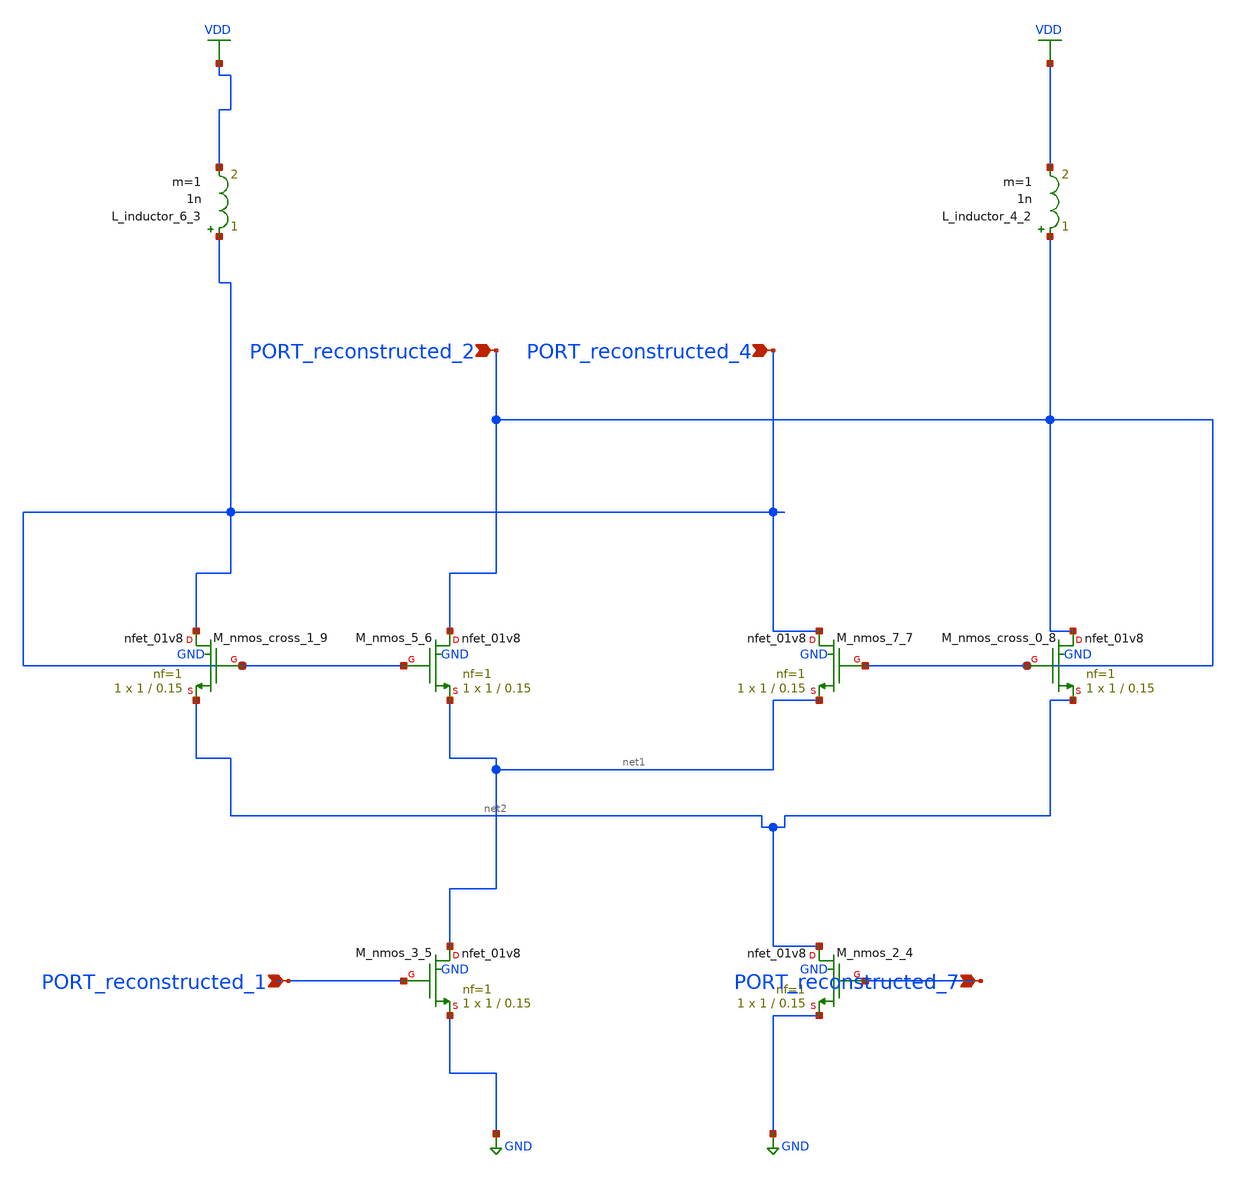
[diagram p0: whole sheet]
** sch_path: schematics/10_1007_s10470-024-02258-z_02_001.sch
**.subckt 10_1007_s10470-024-02258-z_02_001 PORT_reconstructed_2 PORT_reconstructed_1
*+ PORT_reconstructed_4 PORT_reconstructed_7
*.ipin PORT_reconstructed_2
*.ipin PORT_reconstructed_1
*.ipin PORT_reconstructed_4
*.ipin PORT_reconstructed_7
L_inductor_4_2 PORT_reconstructed_2 VDD 1n m=1
L_inductor_6_3 PORT_reconstructed_4 VDD 1n m=1
XM_nmos_2_4 net2 PORT_reconstructed_7 GND GND sky130_fd_pr__nfet_01v8 L=0.15 W=1 nf=1 ad='int((1 + 1)/2) * 1 / 1 * 0.29'
+ as='int((1 + 2)/2) * 1 / 1 * 0.29' pd='2*int((1 + 1)/2) * (1 / 1 + 0.29)' ps='2*int((1 + 2)/2) * (1 / 1 + 0.29)'
+ nrd='0.29 / 1 ' nrs='0.29 / 1 ' sa=0 sb=0 sd=0 mult=1 m=1
XM_nmos_3_5 net1 PORT_reconstructed_1 GND GND sky130_fd_pr__nfet_01v8 L=0.15 W=1 nf=1 ad='int((1 + 1)/2) * 1 / 1 * 0.29'
+ as='int((1 + 2)/2) * 1 / 1 * 0.29' pd='2*int((1 + 1)/2) * (1 / 1 + 0.29)' ps='2*int((1 + 2)/2) * (1 / 1 + 0.29)'
+ nrd='0.29 / 1 ' nrs='0.29 / 1 ' sa=0 sb=0 sd=0 mult=1 m=1
XM_nmos_5_6 PORT_reconstructed_2 PORT_reconstructed_4 net1 GND sky130_fd_pr__nfet_01v8 L=0.15 W=1 nf=1
+ ad='int((1 + 1)/2) * 1 / 1 * 0.29' as='int((1 + 2)/2) * 1 / 1 * 0.29' pd='2*int((1 + 1)/2) * (1 / 1 + 0.29)'
+ ps='2*int((1 + 2)/2) * (1 / 1 + 0.29)' nrd='0.29 / 1 ' nrs='0.29 / 1 ' sa=0 sb=0 sd=0 mult=1 m=1
XM_nmos_7_7 PORT_reconstructed_4 PORT_reconstructed_2 net1 GND sky130_fd_pr__nfet_01v8 L=0.15 W=1 nf=1
+ ad='int((1 + 1)/2) * 1 / 1 * 0.29' as='int((1 + 2)/2) * 1 / 1 * 0.29' pd='2*int((1 + 1)/2) * (1 / 1 + 0.29)'
+ ps='2*int((1 + 2)/2) * (1 / 1 + 0.29)' nrd='0.29 / 1 ' nrs='0.29 / 1 ' sa=0 sb=0 sd=0 mult=1 m=1
XM_nmos_cross_0_8 PORT_reconstructed_2 PORT_reconstructed_2 net2 GND sky130_fd_pr__nfet_01v8 L=0.15 W=1
+ nf=1 ad='int((1 + 1)/2) * 1 / 1 * 0.29' as='int((1 + 2)/2) * 1 / 1 * 0.29' pd='2*int((1 + 1)/2) * (1 / 1 + 0.29)'
+ ps='2*int((1 + 2)/2) * (1 / 1 + 0.29)' nrd='0.29 / 1 ' nrs='0.29 / 1 ' sa=0 sb=0 sd=0 mult=1 m=1
XM_nmos_cross_1_9 PORT_reconstructed_4 PORT_reconstructed_4 net2 GND sky130_fd_pr__nfet_01v8 L=0.15 W=1
+ nf=1 ad='int((1 + 1)/2) * 1 / 1 * 0.29' as='int((1 + 2)/2) * 1 / 1 * 0.29' pd='2*int((1 + 1)/2) * (1 / 1 + 0.29)'
+ ps='2*int((1 + 2)/2) * (1 / 1 + 0.29)' nrd='0.29 / 1 ' nrs='0.29 / 1 ' sa=0 sb=0 sd=0 mult=1 m=1
**.ends
.GLOBAL GND
.GLOBAL VDD
.end
